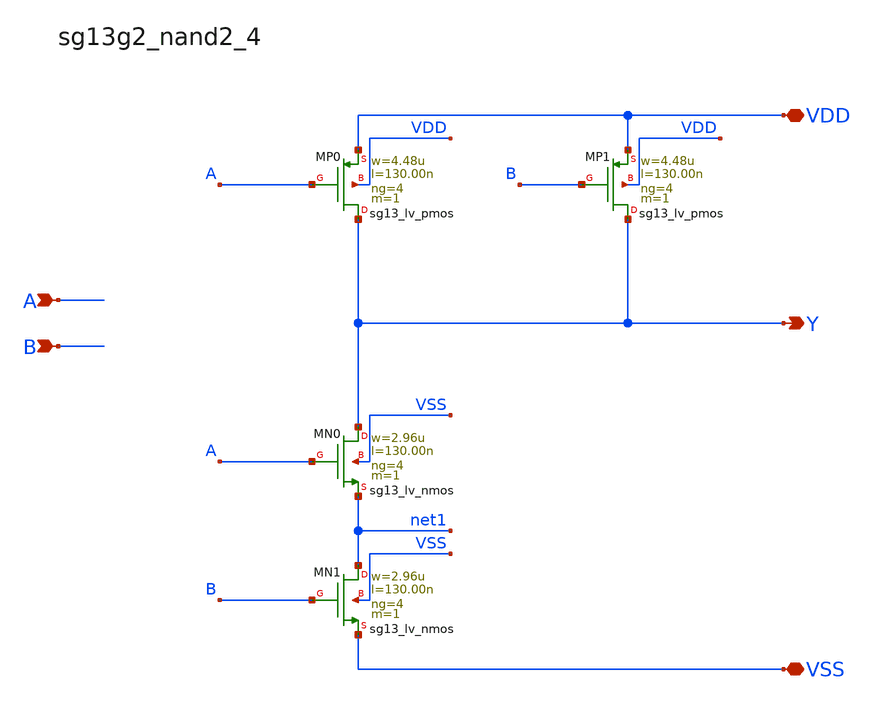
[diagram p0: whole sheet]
** sch_path: outputs/sg13g2_cells/cells/sg13g2_nand2_4/sg13g2_nand2_4.sch
**.subckt sg13g2_nand2_4 Y A B VDD VSS
*.opin Y
*.ipin A
*.ipin B
*.iopin VDD
*.iopin VSS
XMP1 Y B VDD VDD sg13_lv_pmos w=4.48u l=130.00n ng=4 m=1 mm_ok=1
XMP0 Y A VDD VDD sg13_lv_pmos w=4.48u l=130.00n ng=4 m=1 mm_ok=1
XMN1 net1 B VSS VSS sg13_lv_nmos w=2.96u l=130.00n ng=4 m=1 mm_ok=1
XMN0 Y A net1 VSS sg13_lv_nmos w=2.96u l=130.00n ng=4 m=1 mm_ok=1
**.ends
.end
